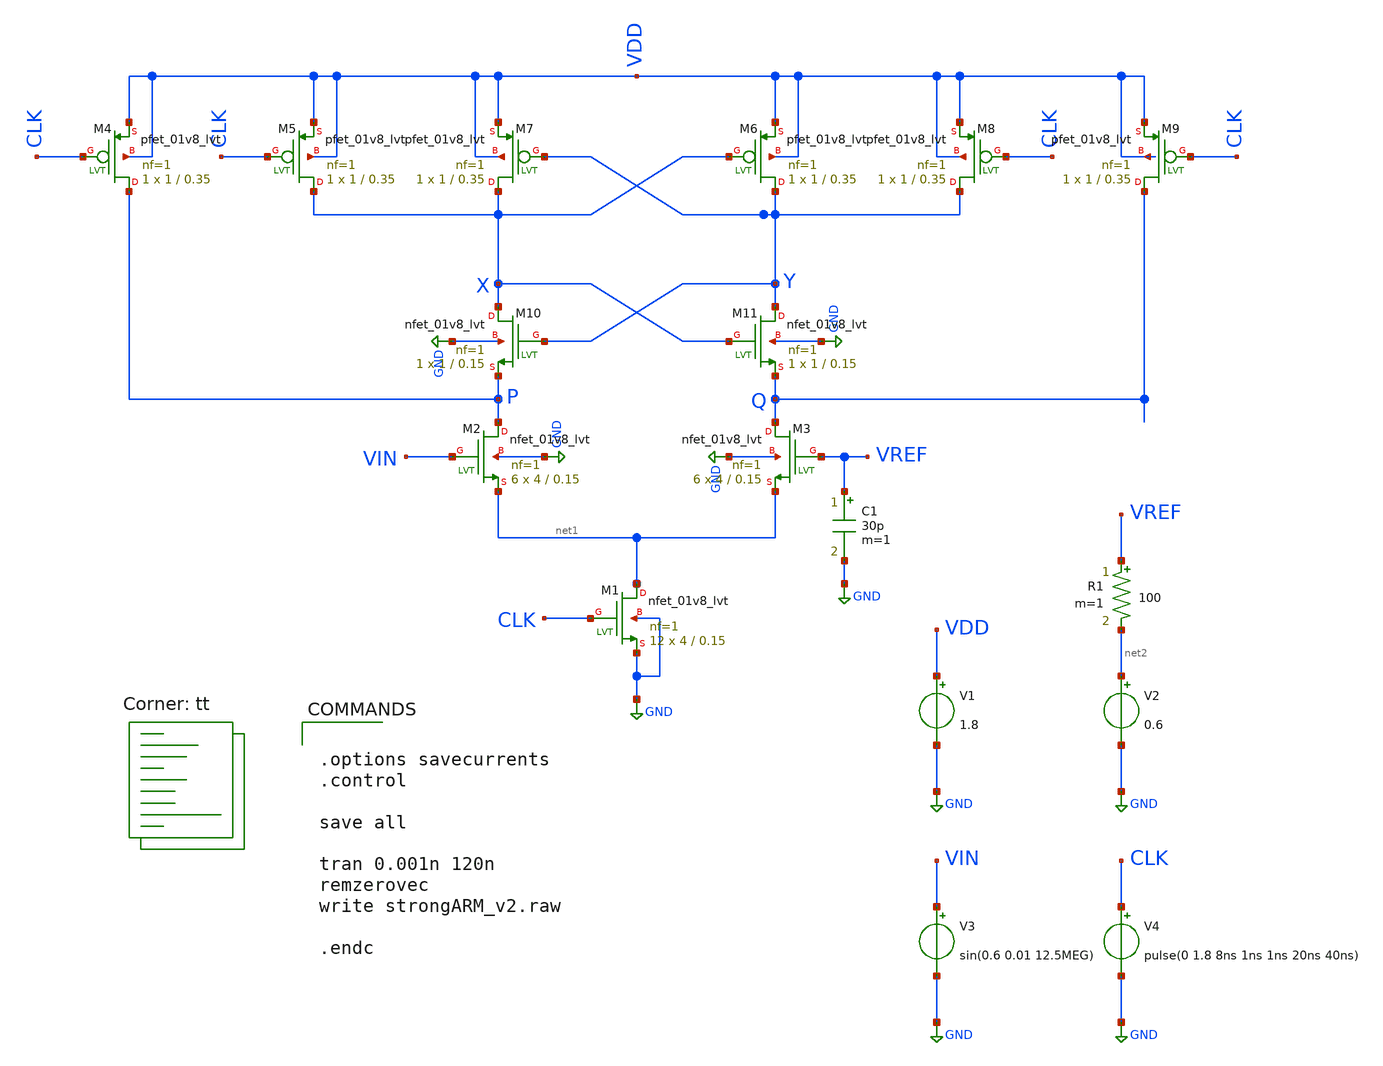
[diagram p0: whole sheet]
** sch_path: strongARM/strongARM_v2.sch
**.subckt strongARM_v2
V1 VDD GND 1.8
V3 VIN GND sin(0.6 0.01 12.5MEG)
V2 net2 GND 0.6
V4 CLK GND pulse(0 1.8 8ns 1ns 1ns 20ns 40ns)
XM2 P VIN net1 GND sky130_fd_pr__nfet_01v8_lvt L=0.15 W=4 nf=1 ad='int((nf+1)/2) * W/nf * 0.29' as='int((nf+2)/2) * W/nf * 0.29'
+ pd='2*int((nf+1)/2) * (W/nf + 0.29)' ps='2*int((nf+2)/2) * (W/nf + 0.29)' nrd='0.29 / W' nrs='0.29 / W'
+ sa=0 sb=0 sd=0 mult=6 m=6
XM3 Q VREF net1 GND sky130_fd_pr__nfet_01v8_lvt L=0.15 W=4 nf=1 ad='int((nf+1)/2) * W/nf * 0.29' as='int((nf+2)/2) * W/nf * 0.29'
+ pd='2*int((nf+1)/2) * (W/nf + 0.29)' ps='2*int((nf+2)/2) * (W/nf + 0.29)' nrd='0.29 / W' nrs='0.29 / W'
+ sa=0 sb=0 sd=0 mult=6 m=6
XM4 P CLK VDD VDD sky130_fd_pr__pfet_01v8_lvt L=0.35 W=1 nf=1 ad='int((nf+1)/2) * W/nf * 0.29' as='int((nf+2)/2) * W/nf * 0.29'
+ pd='2*int((nf+1)/2) * (W/nf + 0.29)' ps='2*int((nf+2)/2) * (W/nf + 0.29)' nrd='0.29 / W' nrs='0.29 / W'
+ sa=0 sb=0 sd=0 mult=1 m=1
XM5 X CLK VDD VDD sky130_fd_pr__pfet_01v8_lvt L=0.35 W=1 nf=1 ad='int((nf+1)/2) * W/nf * 0.29' as='int((nf+2)/2) * W/nf * 0.29'
+ pd='2*int((nf+1)/2) * (W/nf + 0.29)' ps='2*int((nf+2)/2) * (W/nf + 0.29)' nrd='0.29 / W' nrs='0.29 / W'
+ sa=0 sb=0 sd=0 mult=1 m=1
XM6 Y X VDD VDD sky130_fd_pr__pfet_01v8_lvt L=0.35 W=1 nf=1 ad='int((nf+1)/2) * W/nf * 0.29' as='int((nf+2)/2) * W/nf * 0.29'
+ pd='2*int((nf+1)/2) * (W/nf + 0.29)' ps='2*int((nf+2)/2) * (W/nf + 0.29)' nrd='0.29 / W' nrs='0.29 / W'
+ sa=0 sb=0 sd=0 mult=1 m=1
XM7 X Y VDD VDD sky130_fd_pr__pfet_01v8_lvt L=0.35 W=1 nf=1 ad='int((nf+1)/2) * W/nf * 0.29' as='int((nf+2)/2) * W/nf * 0.29'
+ pd='2*int((nf+1)/2) * (W/nf + 0.29)' ps='2*int((nf+2)/2) * (W/nf + 0.29)' nrd='0.29 / W' nrs='0.29 / W'
+ sa=0 sb=0 sd=0 mult=1 m=1
XM8 Y CLK VDD VDD sky130_fd_pr__pfet_01v8_lvt L=0.35 W=1 nf=1 ad='int((nf+1)/2) * W/nf * 0.29' as='int((nf+2)/2) * W/nf * 0.29'
+ pd='2*int((nf+1)/2) * (W/nf + 0.29)' ps='2*int((nf+2)/2) * (W/nf + 0.29)' nrd='0.29 / W' nrs='0.29 / W'
+ sa=0 sb=0 sd=0 mult=1 m=1
XM9 Q CLK VDD VDD sky130_fd_pr__pfet_01v8_lvt L=0.35 W=1 nf=1 ad='int((nf+1)/2) * W/nf * 0.29' as='int((nf+2)/2) * W/nf * 0.29'
+ pd='2*int((nf+1)/2) * (W/nf + 0.29)' ps='2*int((nf+2)/2) * (W/nf + 0.29)' nrd='0.29 / W' nrs='0.29 / W'
+ sa=0 sb=0 sd=0 mult=1 m=1
XM10 X Y P GND sky130_fd_pr__nfet_01v8_lvt L=0.15 W=1 nf=1 ad='int((nf+1)/2) * W/nf * 0.29' as='int((nf+2)/2) * W/nf * 0.29'
+ pd='2*int((nf+1)/2) * (W/nf + 0.29)' ps='2*int((nf+2)/2) * (W/nf + 0.29)' nrd='0.29 / W' nrs='0.29 / W'
+ sa=0 sb=0 sd=0 mult=1 m=1
XM11 Y X Q GND sky130_fd_pr__nfet_01v8_lvt L=0.15 W=1 nf=1 ad='int((nf+1)/2) * W/nf * 0.29' as='int((nf+2)/2) * W/nf * 0.29'
+ pd='2*int((nf+1)/2) * (W/nf + 0.29)' ps='2*int((nf+2)/2) * (W/nf + 0.29)' nrd='0.29 / W' nrs='0.29 / W'
+ sa=0 sb=0 sd=0 mult=1 m=1
XM1 net1 CLK GND GND sky130_fd_pr__nfet_01v8_lvt L=0.15 W=4 nf=1 ad='int((nf+1)/2) * W/nf * 0.29' as='int((nf+2)/2) * W/nf * 0.29'
+ pd='2*int((nf+1)/2) * (W/nf + 0.29)' ps='2*int((nf+2)/2) * (W/nf + 0.29)' nrd='0.29 / W' nrs='0.29 / W'
+ sa=0 sb=0 sd=0 mult=12 m=12
R1 VREF net2 100 m=1
C1 VREF GND 30p m=1
**** begin user architecture code
.lib $::SKYWATER_MODELS/sky130.lib.spice tt


.options savecurrents
.control

save all

tran 0.001n 120n
remzerovec
write strongARM_v2.raw

.endc


**** end user architecture code
**.ends
.GLOBAL GND
.end
